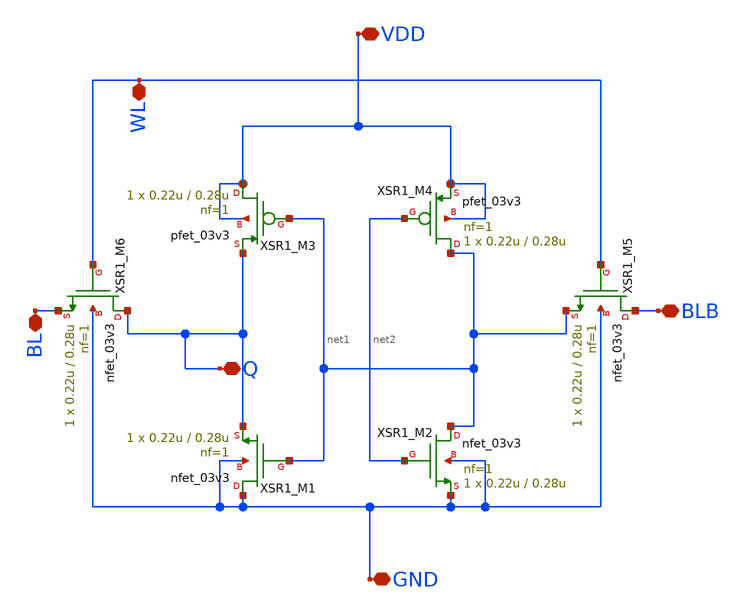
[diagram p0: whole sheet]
** sch_path: src/schematic/6T4BIT/6T4bit.sch
**.subckt 6T4bit BLB GND Q VDD BL WL
*.iopin BLB
*.iopin GND
*.iopin Q
*.iopin VDD
*.iopin BL
*.iopin WL
XSR1_M6 Q WL BL GND nfet_03v3 L=0.28u W=0.22u nf=1 ad='int((nf+1)/2) * W/nf * 0.18u' as='int((nf+2)/2) * W/nf * 0.18u'
+ pd='2*int((nf+1)/2) * (W/nf + 0.18u)' ps='2*int((nf+2)/2) * (W/nf + 0.18u)' nrd='0.18u / W' nrs='0.18u / W'
+ sa=0 sb=0 sd=0 m=1
XSR1_M3 VDD net1 Q VDD pfet_03v3 L=0.28u W=0.22u nf=1 ad='int((nf+1)/2) * W/nf * 0.18u' as='int((nf+2)/2) * W/nf * 0.18u'
+ pd='2*int((nf+1)/2) * (W/nf + 0.18u)' ps='2*int((nf+2)/2) * (W/nf + 0.18u)' nrd='0.18u / W' nrs='0.18u / W'
+ sa=0 sb=0 sd=0 m=1
XSR1_M4 net1 net2 VDD VDD pfet_03v3 L=0.28u W=0.22u nf=1 ad='int((nf+1)/2) * W/nf * 0.18u' as='int((nf+2)/2) * W/nf * 0.18u'
+ pd='2*int((nf+1)/2) * (W/nf + 0.18u)' ps='2*int((nf+2)/2) * (W/nf + 0.18u)' nrd='0.18u / W' nrs='0.18u / W'
+ sa=0 sb=0 sd=0 m=1
XSR1_M5 BLB WL net1 GND nfet_03v3 L=0.28u W=0.22u nf=1 ad='int((nf+1)/2) * W/nf * 0.18u' as='int((nf+2)/2) * W/nf * 0.18u'
+ pd='2*int((nf+1)/2) * (W/nf + 0.18u)' ps='2*int((nf+2)/2) * (W/nf + 0.18u)' nrd='0.18u / W' nrs='0.18u / W'
+ sa=0 sb=0 sd=0 m=1
XSR1_M1 GND net1 Q GND nfet_03v3 L=0.28u W=0.22u nf=1 ad='int((nf+1)/2) * W/nf * 0.18u' as='int((nf+2)/2) * W/nf * 0.18u'
+ pd='2*int((nf+1)/2) * (W/nf + 0.18u)' ps='2*int((nf+2)/2) * (W/nf + 0.18u)' nrd='0.18u / W' nrs='0.18u / W'
+ sa=0 sb=0 sd=0 m=1
XSR1_M2 net1 net2 GND GND nfet_03v3 L=0.28u W=0.22u nf=1 ad='int((nf+1)/2) * W/nf * 0.18u' as='int((nf+2)/2) * W/nf * 0.18u'
+ pd='2*int((nf+1)/2) * (W/nf + 0.18u)' ps='2*int((nf+2)/2) * (W/nf + 0.18u)' nrd='0.18u / W' nrs='0.18u / W'
+ sa=0 sb=0 sd=0 m=1
**.ends
.end
